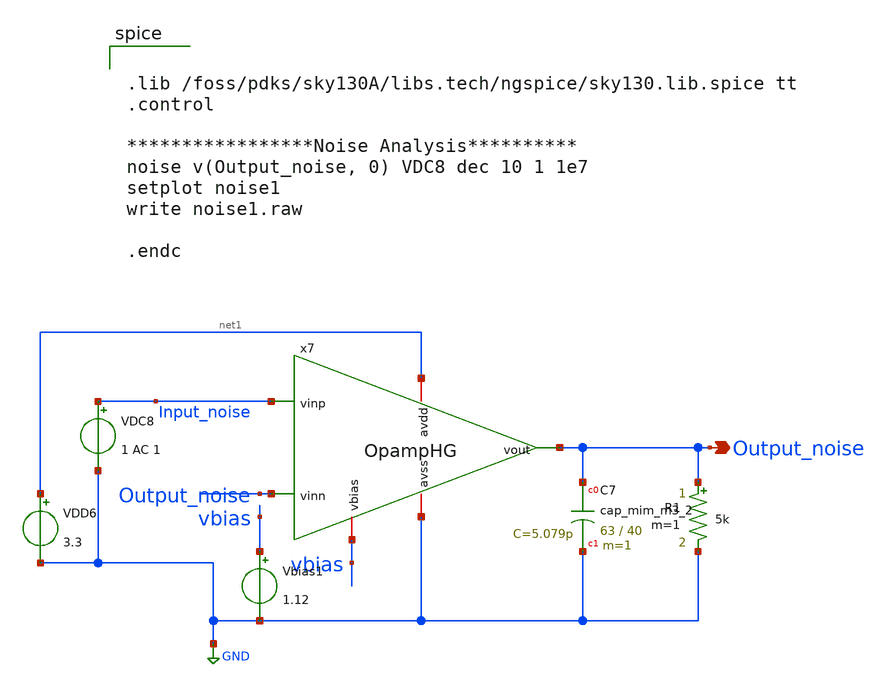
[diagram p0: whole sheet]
** sch_path: OpampHG_noise.sch
**.subckt OpampHG_noise Output_noise
*.opin Output_noise
R1 Output_noise GND 5k m=1
x7 net1 GND vbias Input_noise Output_noise Output_noise OpampHG
VDD6 net1 GND 3.3
VDC8 Input_noise GND 1 AC 1
XC7 Output_noise GND sky130_fd_pr__cap_mim_m3_2 W=63 L=40 MF=1 m=1
Vbias1 vbias GND 1.12
**** begin user architecture code


.lib /foss/pdks/sky130A/libs.tech/ngspice/sky130.lib.spice tt
.control

*****************Noise Analysis**********
noise v(Output_noise, 0) VDC8 dec 10 1 1e7
setplot noise1
write noise1.raw

.endc


**** end user architecture code
**.ends

* expanding   symbol:  /foss/designs/Opamp_HG/OpampHG.sym # of pins=6
** sym_path: OpampHG.sym
** sch_path: OpampHG.sch
.subckt OpampHG avdd avss vbias vinp vinn vout
*.iopin avdd
*.iopin avss
*.iopin vbias
*.ipin vinp
*.ipin vinn
*.opin vout
XC1 net2 Vout_prior sky130_fd_pr__cap_mim_m3_1 W=13 L=9.9 MF=1 m=1
XC2 net3 vout sky130_fd_pr__cap_mim_m3_2 W=20 L=37 MF=1 m=1
XM1 net1 net2 avdd avdd sky130_fd_pr__pfet_01v8 L=0.3 W=5 nf=1 ad='int((nf+1)/2) * W/nf * 0.29' as='int((nf+2)/2) * W/nf * 0.29'
+ pd='2*int((nf+1)/2) * (W/nf + 0.29)' ps='2*int((nf+2)/2) * (W/nf + 0.29)' nrd='0.29 / W' nrs='0.29 / W'
+ sa=0 sb=0 sd=0 mult=1 m=1
XM2 net3 net2 avdd avdd sky130_fd_pr__pfet_01v8 L=0.3 W=5 nf=1 ad='int((nf+1)/2) * W/nf * 0.29' as='int((nf+2)/2) * W/nf * 0.29'
+ pd='2*int((nf+1)/2) * (W/nf + 0.29)' ps='2*int((nf+2)/2) * (W/nf + 0.29)' nrd='0.29 / W' nrs='0.29 / W'
+ sa=0 sb=0 sd=0 mult=1 m=1
XM3 net2 net2 net1 avdd sky130_fd_pr__pfet_01v8 L=0.3 W=5 nf=1 ad='int((nf+1)/2) * W/nf * 0.29' as='int((nf+2)/2) * W/nf * 0.29'
+ pd='2*int((nf+1)/2) * (W/nf + 0.29)' ps='2*int((nf+2)/2) * (W/nf + 0.29)' nrd='0.29 / W' nrs='0.29 / W'
+ sa=0 sb=0 sd=0 mult=1 m=1
XM4 net5 net2 net3 avdd sky130_fd_pr__pfet_01v8 L=0.3 W=5 nf=1 ad='int((nf+1)/2) * W/nf * 0.29' as='int((nf+2)/2) * W/nf * 0.29'
+ pd='2*int((nf+1)/2) * (W/nf + 0.29)' ps='2*int((nf+2)/2) * (W/nf + 0.29)' nrd='0.29 / W' nrs='0.29 / W'
+ sa=0 sb=0 sd=0 mult=1 m=1
XM5 net7 net6 avdd avdd sky130_fd_pr__pfet_01v8 L=0.3 W=5 nf=1 ad='int((nf+1)/2) * W/nf * 0.29' as='int((nf+2)/2) * W/nf * 0.29'
+ pd='2*int((nf+1)/2) * (W/nf + 0.29)' ps='2*int((nf+2)/2) * (W/nf + 0.29)' nrd='0.29 / W' nrs='0.29 / W'
+ sa=0 sb=0 sd=0 mult=1 m=1
XM6 net8 net6 avdd avdd sky130_fd_pr__pfet_01v8 L=0.3 W=5 nf=1 ad='int((nf+1)/2) * W/nf * 0.29' as='int((nf+2)/2) * W/nf * 0.29'
+ pd='2*int((nf+1)/2) * (W/nf + 0.29)' ps='2*int((nf+2)/2) * (W/nf + 0.29)' nrd='0.29 / W' nrs='0.29 / W'
+ sa=0 sb=0 sd=0 mult=1 m=1
XM7 net6 net6 net7 avdd sky130_fd_pr__pfet_01v8 L=0.3 W=5 nf=1 ad='int((nf+1)/2) * W/nf * 0.29' as='int((nf+2)/2) * W/nf * 0.29'
+ pd='2*int((nf+1)/2) * (W/nf + 0.29)' ps='2*int((nf+2)/2) * (W/nf + 0.29)' nrd='0.29 / W' nrs='0.29 / W'
+ sa=0 sb=0 sd=0 mult=1 m=1
XM8 Vout_prior net6 net8 avdd sky130_fd_pr__pfet_01v8 L=0.3 W=5 nf=1 ad='int((nf+1)/2) * W/nf * 0.29'
+ as='int((nf+2)/2) * W/nf * 0.29' pd='2*int((nf+1)/2) * (W/nf + 0.29)' ps='2*int((nf+2)/2) * (W/nf + 0.29)'
+ nrd='0.29 / W' nrs='0.29 / W' sa=0 sb=0 sd=0 mult=1 m=1
XM9 net11 Vout_prior avdd avdd sky130_fd_pr__pfet_01v8 L=0.3 W=50 nf=1 ad='int((nf+1)/2) * W/nf * 0.29'
+ as='int((nf+2)/2) * W/nf * 0.29' pd='2*int((nf+1)/2) * (W/nf + 0.29)' ps='2*int((nf+2)/2) * (W/nf + 0.29)'
+ nrd='0.29 / W' nrs='0.29 / W' sa=0 sb=0 sd=0 mult=1 m=1
XM10 vout Vout_prior net11 avdd sky130_fd_pr__pfet_01v8 L=0.3 W=50 nf=1 ad='int((nf+1)/2) * W/nf * 0.29'
+ as='int((nf+2)/2) * W/nf * 0.29' pd='2*int((nf+1)/2) * (W/nf + 0.29)' ps='2*int((nf+2)/2) * (W/nf + 0.29)'
+ nrd='0.29 / W' nrs='0.29 / W' sa=0 sb=0 sd=0 mult=1 m=1
XM11 net2 vinn net4 avss sky130_fd_pr__nfet_01v8 L=2 W=5 nf=1 ad='int((nf+1)/2) * W/nf * 0.29' as='int((nf+2)/2) * W/nf * 0.29'
+ pd='2*int((nf+1)/2) * (W/nf + 0.29)' ps='2*int((nf+2)/2) * (W/nf + 0.29)' nrd='0.29 / W' nrs='0.29 / W'
+ sa=0 sb=0 sd=0 mult=1 m=1
XM12 net5 vinp net4 avss sky130_fd_pr__nfet_01v8 L=2 W=5 nf=1 ad='int((nf+1)/2) * W/nf * 0.29' as='int((nf+2)/2) * W/nf * 0.29'
+ pd='2*int((nf+1)/2) * (W/nf + 0.29)' ps='2*int((nf+2)/2) * (W/nf + 0.29)' nrd='0.29 / W' nrs='0.29 / W'
+ sa=0 sb=0 sd=0 mult=1 m=1
XM13 net6 net5 net10 avss sky130_fd_pr__nfet_01v8 L=2 W=5 nf=1 ad='int((nf+1)/2) * W/nf * 0.29' as='int((nf+2)/2) * W/nf * 0.29'
+ pd='2*int((nf+1)/2) * (W/nf + 0.29)' ps='2*int((nf+2)/2) * (W/nf + 0.29)' nrd='0.29 / W' nrs='0.29 / W'
+ sa=0 sb=0 sd=0 mult=1 m=1
XM14 Vout_prior net2 net9 avss sky130_fd_pr__nfet_01v8 L=2 W=5 nf=1 ad='int((nf+1)/2) * W/nf * 0.29'
+ as='int((nf+2)/2) * W/nf * 0.29' pd='2*int((nf+1)/2) * (W/nf + 0.29)' ps='2*int((nf+2)/2) * (W/nf + 0.29)'
+ nrd='0.29 / W' nrs='0.29 / W' sa=0 sb=0 sd=0 mult=1 m=1
XM15 net4 vbias avss avss sky130_fd_pr__nfet_01v8 L=0.6 W=2.6 nf=1 ad='int((nf+1)/2) * W/nf * 0.29' as='int((nf+2)/2) * W/nf * 0.29'
+ pd='2*int((nf+1)/2) * (W/nf + 0.29)' ps='2*int((nf+2)/2) * (W/nf + 0.29)' nrd='0.29 / W' nrs='0.29 / W'
+ sa=0 sb=0 sd=0 mult=1 m=1
XM16 net4 vbias avss avss sky130_fd_pr__nfet_01v8 L=0.6 W=2.6 nf=1 ad='int((nf+1)/2) * W/nf * 0.29' as='int((nf+2)/2) * W/nf * 0.29'
+ pd='2*int((nf+1)/2) * (W/nf + 0.29)' ps='2*int((nf+2)/2) * (W/nf + 0.29)' nrd='0.29 / W' nrs='0.29 / W'
+ sa=0 sb=0 sd=0 mult=1 m=1
XM17 net10 vbias avss avss sky130_fd_pr__nfet_01v8 L=0.6 W=2.6 nf=1 ad='int((nf+1)/2) * W/nf * 0.29'
+ as='int((nf+2)/2) * W/nf * 0.29' pd='2*int((nf+1)/2) * (W/nf + 0.29)' ps='2*int((nf+2)/2) * (W/nf + 0.29)'
+ nrd='0.29 / W' nrs='0.29 / W' sa=0 sb=0 sd=0 mult=1 m=1
XM18 net9 vbias avss avss sky130_fd_pr__nfet_01v8 L=0.6 W=2.6 nf=1 ad='int((nf+1)/2) * W/nf * 0.29' as='int((nf+2)/2) * W/nf * 0.29'
+ pd='2*int((nf+1)/2) * (W/nf + 0.29)' ps='2*int((nf+2)/2) * (W/nf + 0.29)' nrd='0.29 / W' nrs='0.29 / W'
+ sa=0 sb=0 sd=0 mult=1 m=1
XM19 vout vbias avss avss sky130_fd_pr__nfet_01v8 L=0.6 W=20.4 nf=1 ad='int((nf+1)/2) * W/nf * 0.29'
+ as='int((nf+2)/2) * W/nf * 0.29' pd='2*int((nf+1)/2) * (W/nf + 0.29)' ps='2*int((nf+2)/2) * (W/nf + 0.29)'
+ nrd='0.29 / W' nrs='0.29 / W' sa=0 sb=0 sd=0 mult=1 m=1
.ends

.GLOBAL GND
.end
